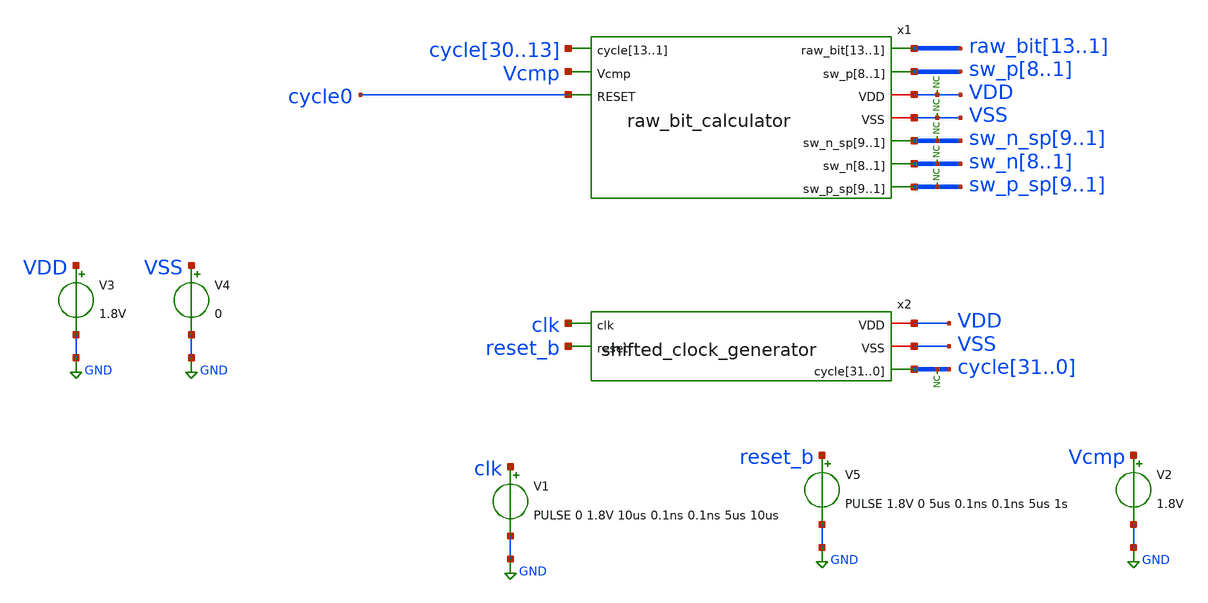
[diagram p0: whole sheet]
** sch_path: xschem/tests/raw_bit_calculator/raw_bit_calculator_test.sch
**.subckt raw_bit_calculator_test
V3 VDD GND 1.8V
V4 VSS GND 0
x1 raw_bit13 raw_bit12 raw_bit11 raw_bit10 raw_bit9 raw_bit8 raw_bit7 raw_bit6 raw_bit5 raw_bit4
+ raw_bit3 raw_bit2 raw_bit1 cycle30 cycle29 cycle28 cycle27 cycle26 cycle25 cycle24 cycle23 cycle22 cycle21
+ cycle20 cycle19 cycle18 sw_p8 sw_p7 sw_p6 sw_p5 sw_p4 sw_p3 sw_p2 sw_p1 Vcmp cycle0 VDD VSS sw_n_sp9
+ sw_n_sp8 sw_n_sp7 sw_n_sp6 sw_n_sp5 sw_n_sp4 sw_n_sp3 sw_n_sp2 sw_n_sp1 sw_n8 sw_n7 sw_n6 sw_n5 sw_n4 sw_n3
+ sw_n2 sw_n1 sw_p_sp9 sw_p_sp8 sw_p_sp7 sw_p_sp6 sw_p_sp5 sw_p_sp4 sw_p_sp3 sw_p_sp2 sw_p_sp1
+ raw_bit_calculator
* noconn cycle[31..0]
V1 clk GND PULSE 0 1.8V 10us 0.1ns 0.1ns 5us 10us
V5 reset_b GND PULSE 1.8V 0 5us 0.1ns 0.1ns 5us 1s
V2 Vcmp GND 1.8V
* noconn VDD
* noconn VSS
* noconn sw_n_sp[9..1]
* noconn sw_n[8..1]
* noconn sw_p_sp[9..1]
x2 clk VDD VSS reset_b cycle31 cycle30 cycle29 cycle28 cycle27 cycle26 cycle25 cycle24 cycle23
+ cycle22 cycle21 cycle20 cycle19 cycle18 cycle17 cycle16 cycle15 cycle14 cycle13 cycle12 cycle11 cycle10
+ cycle9 cycle8 cycle7 cycle6 cycle5 cycle4 cycle3 cycle2 cycle1 cycle0 shifted_clock_generator
**** begin user architecture code
 .lib $::SKYWATER_MODELS/sky130.lib.spice tt
.include $::SKYWATER_STDCELLS/sky130_fd_sc_hd.spice


.options acct list
.temp 25
*vvcc VDD 0 dc 1.8
*vvss VSS 0 0
.control
tran 0.1u 400u
plot cycle0-2 sw_n_sp1 sw_n_sp2+2 sw_n_sp3+4 sw_n_sp4+6 sw_n_sp5+8 sw_n_sp6+10 sw_n_sp7+12
+ sw_n_sp8+14 sw_n_sp9+16
plot cycle0-2 sw_p_sp1 sw_p_sp2+2 sw_p_sp3+4 sw_p_sp4+6 sw_p_sp5+8 sw_p_sp6+10 sw_p_sp7+12
+ sw_p_sp8+14 sw_p_sp9+16
plot cycle0-2 sw_n1 sw_n2+2 sw_n3+4 sw_n4+6 sw_n5+8 sw_n6+10 sw_n7+12 sw_n8+14
plot cycle0-2 sw_p1 sw_p2+2 sw_p3+4 sw_p4+6 sw_p5+8 sw_p6+10 sw_p7+12 sw_p8+14
plot raw_bit1 raw_bit2+2 raw_bit3+4 raw_bit4+6 raw_bit5+8 raw_bit6+10 raw_bit7+12 raw_bit8+14
+ raw_bit9+16 raw_bit10+18
plot reset_b-6 clk-4 cycle0 cycle1+2 cycle2+4 cycle3+6 cycle4+8 cycle5+10 cycle6+12 cycle7+14
+ cycle8+16 cycle9+18 cycle10+20 cycle11+22 cycle12+24 cycle13+26 cycle14+28 cycle15+30 cycle16+32 cycle17+34
+ cycle18+36 cycle19+38 cycle20+40 cycle21+42 cycle22+44  cycle23+46 cycle24+48 cycle25+50 cycle26+52 cycle27+54
+ cycle28+56 cycle29+58 cycle30+60 cycle31+62

write raw_bit_calculator_test.raw
.endc


**** end user architecture code
**.ends
.GLOBAL GND
.end
